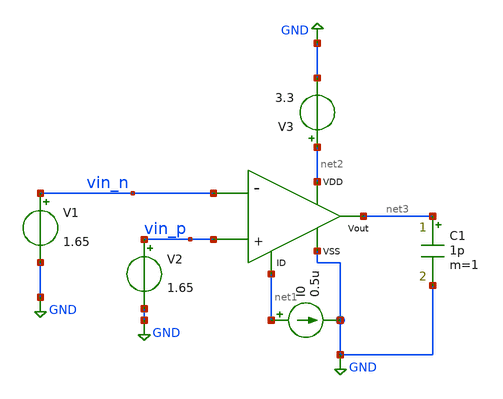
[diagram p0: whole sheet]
** sch_path: xschem/ota_miller/prueba_ota_p_in.sch
**.subckt prueba_ota_p_in
V1 vin_n GND 1.65
I0 net1 GND 0.5u
V2 vin_p GND 1.65
V3 net2 GND 3.3
x1 net2 net1 vin_p vin_n net3 GND ota_p_in
C1 net3 GND 1p m=1
**** begin user architecture code


.control
* ======================= ESTILO DE GRAFICOS =======================
set color0=white
set color1=black
set color2=blue
set color3=red
set xbrushwidth=2

* ==================================================================
* 1. UMBRALES GENERALES, FUENTES, DIMENSIONES, m Y nf EDITABLES
* ==================================================================
set gmid_debil  = 15
set gmid_fuerte = 10
set sat_min     = 0.1

set v1_val  = 0.4
set v2_val  = 0.4
set v3_val  = 3.3
set i0_val  = 0.5e-6

set w1_val = 29e-6   set l1_val = 1e-6   set m1_val = 1   set nf1_val = 1
set w2_val = 29e-6   set l2_val = 1e-6   set m2_val = 1   set nf2_val = 1
set w3_val = 0.22e-6   set l3_val = 1.6e-6   set m3_val = 1   set nf3_val = 1
set w4_val = 0.22e-6   set l4_val = 1.6e-6   set m4_val = 1   set nf4_val = 1
set w5_val = 1e-6   set l5_val = 1e-6   set m5_val = 4   set nf5_val = 1
set w6_val = 1e-6   set l6_val = 1e-6   set m6_val = 1   set nf6_val = 1

* Si w1..w6 estan definidos a nivel donde alterparam los alcanza, descomenta:
* alterparam w1=$w1_val l1=$l1_val m1=$m1_val nf1=$nf1_val
* alterparam w2=$w2_val l2=$l2_val m2=$m2_val nf2=$nf2_val
* alterparam w3=$w3_val l3=$l3_val m3=$m3_val nf3=$nf3_val
* alterparam w4=$w4_val l4=$l4_val m4=$m4_val nf4=$nf4_val
* alterparam w5=$w5_val l5=$l5_val m5=$m5_val nf5=$nf5_val
* alterparam w6=$w6_val l6=$l6_val m6=$m6_val nf6=$nf6_val
* reset

* ==================================================================
* 2. GUARDAR PARAMETROS INTERNOS, FIJAR FUENTES Y CORRER OP
* ==================================================================
save all
save @m.x1.m.xm1.m0[id] @m.x1.m.xm1.m0[gm] @m.x1.m.xm1.m0[gds] @m.x1.m.xm1.m0[vds]
+ @m.x1.m.xm1.m0[vdsat] @m.x1.m.xm1.m0[vgs]
save @m.x1.m.xm2.m0[id] @m.x1.m.xm2.m0[gm] @m.x1.m.xm2.m0[gds] @m.x1.m.xm2.m0[vds]
+ @m.x1.m.xm2.m0[vdsat] @m.x1.m.xm2.m0[vgs]
save @m.x1.m.xm3.m0[id] @m.x1.m.xm3.m0[gm] @m.x1.m.xm3.m0[gds] @m.x1.m.xm3.m0[vds]
+ @m.x1.m.xm3.m0[vdsat] @m.x1.m.xm3.m0[vgs]
save @m.x1.m.xm4.m0[id] @m.x1.m.xm4.m0[gm] @m.x1.m.xm4.m0[gds] @m.x1.m.xm4.m0[vds]
+ @m.x1.m.xm4.m0[vdsat] @m.x1.m.xm4.m0[vgs]
save @m.x1.m.xm5.m0[id] @m.x1.m.xm5.m0[gm] @m.x1.m.xm5.m0[gds] @m.x1.m.xm5.m0[vds]
+ @m.x1.m.xm5.m0[vdsat] @m.x1.m.xm5.m0[vgs]
save @m.x1.m.xm6.m0[id] @m.x1.m.xm6.m0[gm] @m.x1.m.xm6.m0[gds] @m.x1.m.xm6.m0[vds]
+ @m.x1.m.xm6.m0[vdsat] @m.x1.m.xm6.m0[vgs]

alter V1 $v1_val
alter V2 $v2_val
alter V3 $v3_val
alter I0 $i0_val

op

* --- XM1 ---
let id1 = abs(@m.x1.m.xm1.m0[id])
let gm1 = abs(@m.x1.m.xm1.m0[gm])
let gmid1 = gm1 / (id1 + 1e-18)
let vds1 = abs(@m.x1.m.xm1.m0[vds])
let vdsat1 = abs(@m.x1.m.xm1.m0[vdsat])
let sat_mrg1 = vds1 - vdsat1

* --- XM2 ---
let id2 = abs(@m.x1.m.xm2.m0[id])
let gm2 = abs(@m.x1.m.xm2.m0[gm])
let gmid2 = gm2 / (id2 + 1e-18)
let vds2 = abs(@m.x1.m.xm2.m0[vds])
let vdsat2 = abs(@m.x1.m.xm2.m0[vdsat])
let sat_mrg2 = vds2 - vdsat2

* --- XM3 ---
let id3 = abs(@m.x1.m.xm3.m0[id])
let gm3 = abs(@m.x1.m.xm3.m0[gm])
let gmid3 = gm3 / (id3 + 1e-18)
let vds3 = abs(@m.x1.m.xm3.m0[vds])
let vdsat3 = abs(@m.x1.m.xm3.m0[vdsat])
let sat_mrg3 = vds3 - vdsat3

* --- XM4 ---
let id4 = abs(@m.x1.m.xm4.m0[id])
let gm4 = abs(@m.x1.m.xm4.m0[gm])
let gmid4 = gm4 / (id4 + 1e-18)
let vds4 = abs(@m.x1.m.xm4.m0[vds])
let vdsat4 = abs(@m.x1.m.xm4.m0[vdsat])
let sat_mrg4 = vds4 - vdsat4

* --- XM5 ---
let id5 = abs(@m.x1.m.xm5.m0[id])
let gm5 = abs(@m.x1.m.xm5.m0[gm])
let gmid5 = gm5 / (id5 + 1e-18)
let vds5 = abs(@m.x1.m.xm5.m0[vds])
let vdsat5 = abs(@m.x1.m.xm5.m0[vdsat])
let sat_mrg5 = vds5 - vdsat5

* --- XM6 ---
let id6 = abs(@m.x1.m.xm6.m0[id])
let gm6 = abs(@m.x1.m.xm6.m0[gm])
let gmid6 = gm6 / (id6 + 1e-18)
let vds6 = abs(@m.x1.m.xm6.m0[vds])
let vdsat6 = abs(@m.x1.m.xm6.m0[vdsat])
let sat_mrg6 = vds6 - vdsat6

echo '============================================================'
echo 'RESUMEN DE INVERSION (gm/ID) Y MARGEN DE SATURACION'
echo '============================================================'

* --- Diagnostico XM1 ---
echo '--- XM1 ---'
print id1 gmid1 sat_mrg1
if gmid1 > $gmid_debil
  echo '  Inversion : DEBIL'
else
  if gmid1 < $gmid_fuerte
    echo '  Inversion : FUERTE'
  else
    echo '  Inversion : MODERADA'
  end
end
if sat_mrg1 >= $sat_min
  echo '  Saturacion: OK (>= umbral minimo)'
else
  if sat_mrg1 >= 0
    echo '  Saturacion: BAJO MARGEN (0 a < umbral minimo)'
  else
    echo '  Saturacion: LINEAL (margen < 0 V)'
  end
end

* --- Diagnostico XM2 ---
echo '--- XM2 ---'
print id2 gmid2 sat_mrg2
if gmid2 > $gmid_debil
  echo '  Inversion : DEBIL'
else
  if gmid2 < $gmid_fuerte
    echo '  Inversion : FUERTE'
  else
    echo '  Inversion : MODERADA'
  end
end
if sat_mrg2 >= $sat_min
  echo '  Saturacion: OK (>= umbral minimo)'
else
  if sat_mrg2 >= 0
    echo '  Saturacion: BAJO MARGEN (0 a < umbral minimo)'
  else
    echo '  Saturacion: LINEAL (margen < 0 V)'
  end
end

* --- Diagnostico XM3 ---
echo '--- XM3 ---'
print id3 gmid3 sat_mrg3
if gmid3 > $gmid_debil
  echo '  Inversion : DEBIL'
else
  if gmid3 < $gmid_fuerte
    echo '  Inversion : FUERTE'
  else
    echo '  Inversion : MODERADA'
  end
end
if sat_mrg3 >= $sat_min
  echo '  Saturacion: OK (>= umbral minimo)'
else
  if sat_mrg3 >= 0
    echo '  Saturacion: BAJO MARGEN (0 a < umbral minimo)'
  else
    echo '  Saturacion: LINEAL (margen < 0 V)'
  end
end

* --- Diagnostico XM4 ---
echo '--- XM4 ---'
print id4 gmid4 sat_mrg4
if gmid4 > $gmid_debil
  echo '  Inversion : DEBIL'
else
  if gmid4 < $gmid_fuerte
    echo '  Inversion : FUERTE'
  else
    echo '  Inversion : MODERADA'
  end
end
if sat_mrg4 >= $sat_min
  echo '  Saturacion: OK (>= umbral minimo)'
else
  if sat_mrg4 >= 0
    echo '  Saturacion: BAJO MARGEN (0 a < umbral minimo)'
  else
    echo '  Saturacion: LINEAL (margen < 0 V)'
  end
end

* --- Diagnostico XM5 ---
echo '--- XM5 ---'
print id5 gmid5 sat_mrg5
if gmid5 > $gmid_debil
  echo '  Inversion : DEBIL'
else
  if gmid5 < $gmid_fuerte
    echo '  Inversion : FUERTE'
  else
    echo '  Inversion : MODERADA'
  end
end
if sat_mrg5 >= $sat_min
  echo '  Saturacion: OK (>= umbral minimo)'
else
  if sat_mrg5 >= 0
    echo '  Saturacion: BAJO MARGEN (0 a < umbral minimo)'
  else
    echo '  Saturacion: LINEAL (margen < 0 V)'
  end
end

* --- Diagnostico XM6 ---
echo '--- XM6 ---'
print id6 gmid6 sat_mrg6
if gmid6 > $gmid_debil
  echo '  Inversion : DEBIL'
else
  if gmid6 < $gmid_fuerte
    echo '  Inversion : FUERTE'
  else
    echo '  Inversion : MODERADA'
  end
end
if sat_mrg6 >= $sat_min
  echo '  Saturacion: OK (>= umbral minimo)'
else
  if sat_mrg6 >= 0
    echo '  Saturacion: BAJO MARGEN (0 a < umbral minimo)'
  else
    echo '  Saturacion: LINEAL (margen < 0 V)'
  end
end

echo '============================================================'

.endc


**** end user architecture code
**.ends

* expanding   symbol:  /home/ringosinye/eda/projects/ldo-gf180/xschem/ota_miller/ota_p_in.sym # of
*+ pins=6
** sym_path: xschem/ota_miller/ota_p_in.sym
** sch_path: xschem/ota_miller/ota_p_in.sch
.subckt ota_p_in VDD ID + - Vout VSS
*.opin Vout
*.ipin VSS
*.ipin VDD
*.ipin +
*.ipin -
*.ipin ID
XM1 net1 + net2 VDD pfet_03v3 L={l1} W={w1} nf={nf1} ad='int((nf+1)/2) * W/nf * 0.18u' as='int((nf+2)/2) * W/nf * 0.18u'
+ pd='2*int((nf+1)/2) * (W/nf + 0.18u)' ps='2*int((nf+2)/2) * (W/nf + 0.18u)' nrd='0.18u / W' nrs='0.18u / W'
+ sa=0 sb=0 sd=0 m={m1} par={m1}
XM2 Vout - net2 VDD pfet_03v3 L={l2} W={w2} nf={nf2} ad='int((nf+1)/2) * W/nf * 0.18u' as='int((nf+2)/2) * W/nf * 0.18u'
+ pd='2*int((nf+1)/2) * (W/nf + 0.18u)' ps='2*int((nf+2)/2) * (W/nf + 0.18u)' nrd='0.18u / W' nrs='0.18u / W'
+ sa=0 sb=0 sd=0 m={m2} par={m2}
XM3 net1 net1 VSS GND nfet_03v3 L={l3} W={w3} nf={nf3} ad='int((nf+1)/2) * W/nf * 0.18u' as='int((nf+2)/2) * W/nf * 0.18u'
+ pd='2*int((nf+1)/2) * (W/nf + 0.18u)' ps='2*int((nf+2)/2) * (W/nf + 0.18u)' nrd='0.18u / W' nrs='0.18u / W'
+ sa=0 sb=0 sd=0 m={m3} par={m3}
XM4 Vout net1 VSS GND nfet_03v3 L={l4} W={w4} nf={nf4} ad='int((nf+1)/2) * W/nf * 0.18u' as='int((nf+2)/2) * W/nf * 0.18u'
+ pd='2*int((nf+1)/2) * (W/nf + 0.18u)' ps='2*int((nf+2)/2) * (W/nf + 0.18u)' nrd='0.18u / W' nrs='0.18u / W'
+ sa=0 sb=0 sd=0 m={m4} par={m4}
XM5 net2 ID VDD VDD pfet_03v3 L={l5} W={w5} nf={nf5} ad='int((nf+1)/2) * W/nf * 0.18u' as='int((nf+2)/2) * W/nf * 0.18u'
+ pd='2*int((nf+1)/2) * (W/nf + 0.18u)' ps='2*int((nf+2)/2) * (W/nf + 0.18u)' nrd='0.18u / W' nrs='0.18u / W'
+ sa=0 sb=0 sd=0 m={m5} par={m5}
XM6 ID ID VDD VDD pfet_03v3 L={l6} W={w6} nf={nf6} ad='int((nf+1)/2) * W/nf * 0.18u' as='int((nf+2)/2) * W/nf * 0.18u'
+ pd='2*int((nf+1)/2) * (W/nf + 0.18u)' ps='2*int((nf+2)/2) * (W/nf + 0.18u)' nrd='0.18u / W' nrs='0.18u / W'
+ sa=0 sb=0 sd=0 m={m6} par={m6}
**** begin user architecture code


.param w1=29u l1=1u m1=1 nf1=1
.param w2=29u l2=1u m2=1 nf2=1
.param w3=0.22u l3=1.6u m3=1 nf3=1
.param w4=0.22u l4=1.6u m4=1 nf4=1
.param w5=1u l5=1u m5=4 nf5=1
.param w6=1u l6=1u m6=1 nf6=1


**** end user architecture code
**** begin user architecture code


.include /home/ringosinye/eda/pdks/gf180mcuD/libs.tech/ngspice/design.ngspice
.lib /home/ringosinye/eda/pdks/gf180mcuD/libs.tech/ngspice/sm141064.ngspice typical


**** end user architecture code
.ends

.GLOBAL GND
.end
